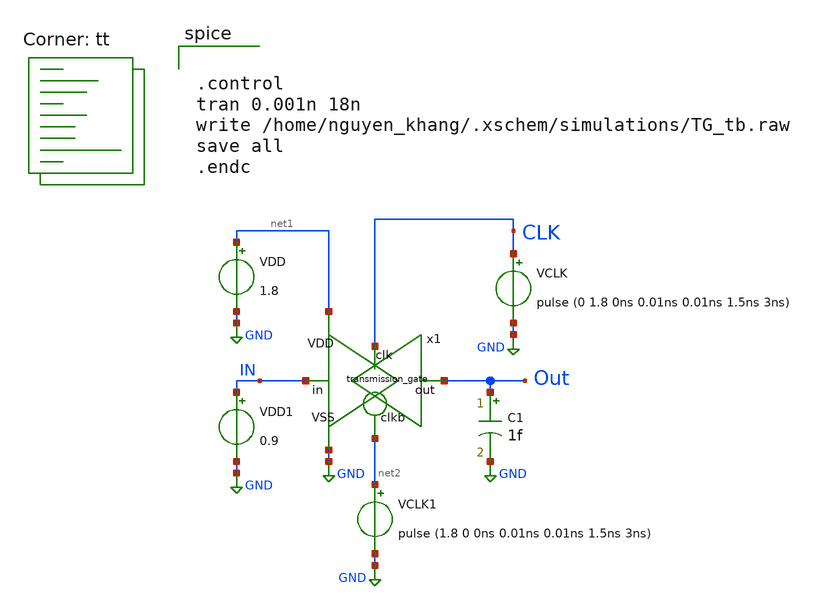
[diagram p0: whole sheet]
** sch_path: transmission_gate_tb.sch
**.subckt transmission_gate_tb
x1 IN net2 CLK net1 GND Out transmission_gate
VDD net1 GND 1.8
VDD1 IN GND 0.9
C1 Out GND 1f m=1
VCLK CLK GND pulse (0 1.8 0ns 0.01ns 0.01ns 1.5ns 3ns)
VCLK1 net2 GND pulse (1.8 0 0ns 0.01ns 0.01ns 1.5ns 3ns)
**** begin user architecture code
.lib $::SKYWATER_MODELS/sky130.lib.spice tt


.control
tran 0.001n 18n
write /home/nguyen_khang/.xschem/simulations/TG_tb.raw
save all
.endc

**** end user architecture code
**.ends

* expanding   symbol:  project/transmission_gate.sym # of pins=6
** sym_path: transmission_gate.sym
** sch_path: transmission_gate.sch
.subckt transmission_gate in clkb clk VDD VSS out
*.ipin in
*.ipin clk
*.ipin clkb
*.opin out
*.ipin VDD
*.ipin VSS
XM1 out clk in VSS sky130_fd_pr__nfet_01v8 L=0.15 W=0.5 nf=1 ad='int((nf+1)/2) * W/nf * 0.29' as='int((nf+2)/2) * W/nf * 0.29'
+ pd='2*int((nf+1)/2) * (W/nf + 0.29)' ps='2*int((nf+2)/2) * (W/nf + 0.29)' nrd='0.29 / W' nrs='0.29 / W'
+ sa=0 sb=0 sd=0 mult=1 m=1
XM2 out clkb in VDD sky130_fd_pr__pfet_01v8 L=0.15 W=0.5 nf=1 ad='int((nf+1)/2) * W/nf * 0.29' as='int((nf+2)/2) * W/nf * 0.29'
+ pd='2*int((nf+1)/2) * (W/nf + 0.29)' ps='2*int((nf+2)/2) * (W/nf + 0.29)' nrd='0.29 / W' nrs='0.29 / W'
+ sa=0 sb=0 sd=0 mult=1 m=1
.ends

.GLOBAL GND
.end
